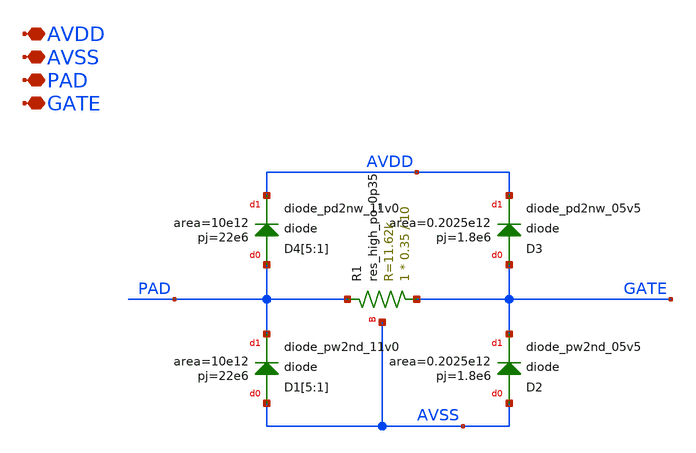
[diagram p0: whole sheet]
** sch_path: xschem/ESD/ESD.sch
**.subckt ESD AVDD AVSS PAD GATE
*.iopin AVDD
*.iopin AVSS
*.iopin PAD
*.iopin GATE
XD2 AVSS GATE sky130_fd_pr__diode_pw2nd_05v5 area=0.2025e12 pj=1.8e6
XD1[5] AVSS PAD sky130_fd_pr__diode_pw2nd_11v0 area=10e12 pj=22e6
XD1[4] AVSS PAD sky130_fd_pr__diode_pw2nd_11v0 area=10e12 pj=22e6
XD1[3] AVSS PAD sky130_fd_pr__diode_pw2nd_11v0 area=10e12 pj=22e6
XD1[2] AVSS PAD sky130_fd_pr__diode_pw2nd_11v0 area=10e12 pj=22e6
XD1[1] AVSS PAD sky130_fd_pr__diode_pw2nd_11v0 area=10e12 pj=22e6
XD3 GATE AVDD sky130_fd_pr__diode_pd2nw_05v5 area=0.2025e12 pj=1.8e6
XD4[5] PAD AVDD sky130_fd_pr__diode_pd2nw_11v0 area=10e12 pj=22e6
XD4[4] PAD AVDD sky130_fd_pr__diode_pd2nw_11v0 area=10e12 pj=22e6
XD4[3] PAD AVDD sky130_fd_pr__diode_pd2nw_11v0 area=10e12 pj=22e6
XD4[2] PAD AVDD sky130_fd_pr__diode_pd2nw_11v0 area=10e12 pj=22e6
XD4[1] PAD AVDD sky130_fd_pr__diode_pd2nw_11v0 area=10e12 pj=22e6
XR1 GATE PAD AVSS sky130_fd_pr__res_high_po_0p35 L=10 mult=1 m=1
**.ends
.end
